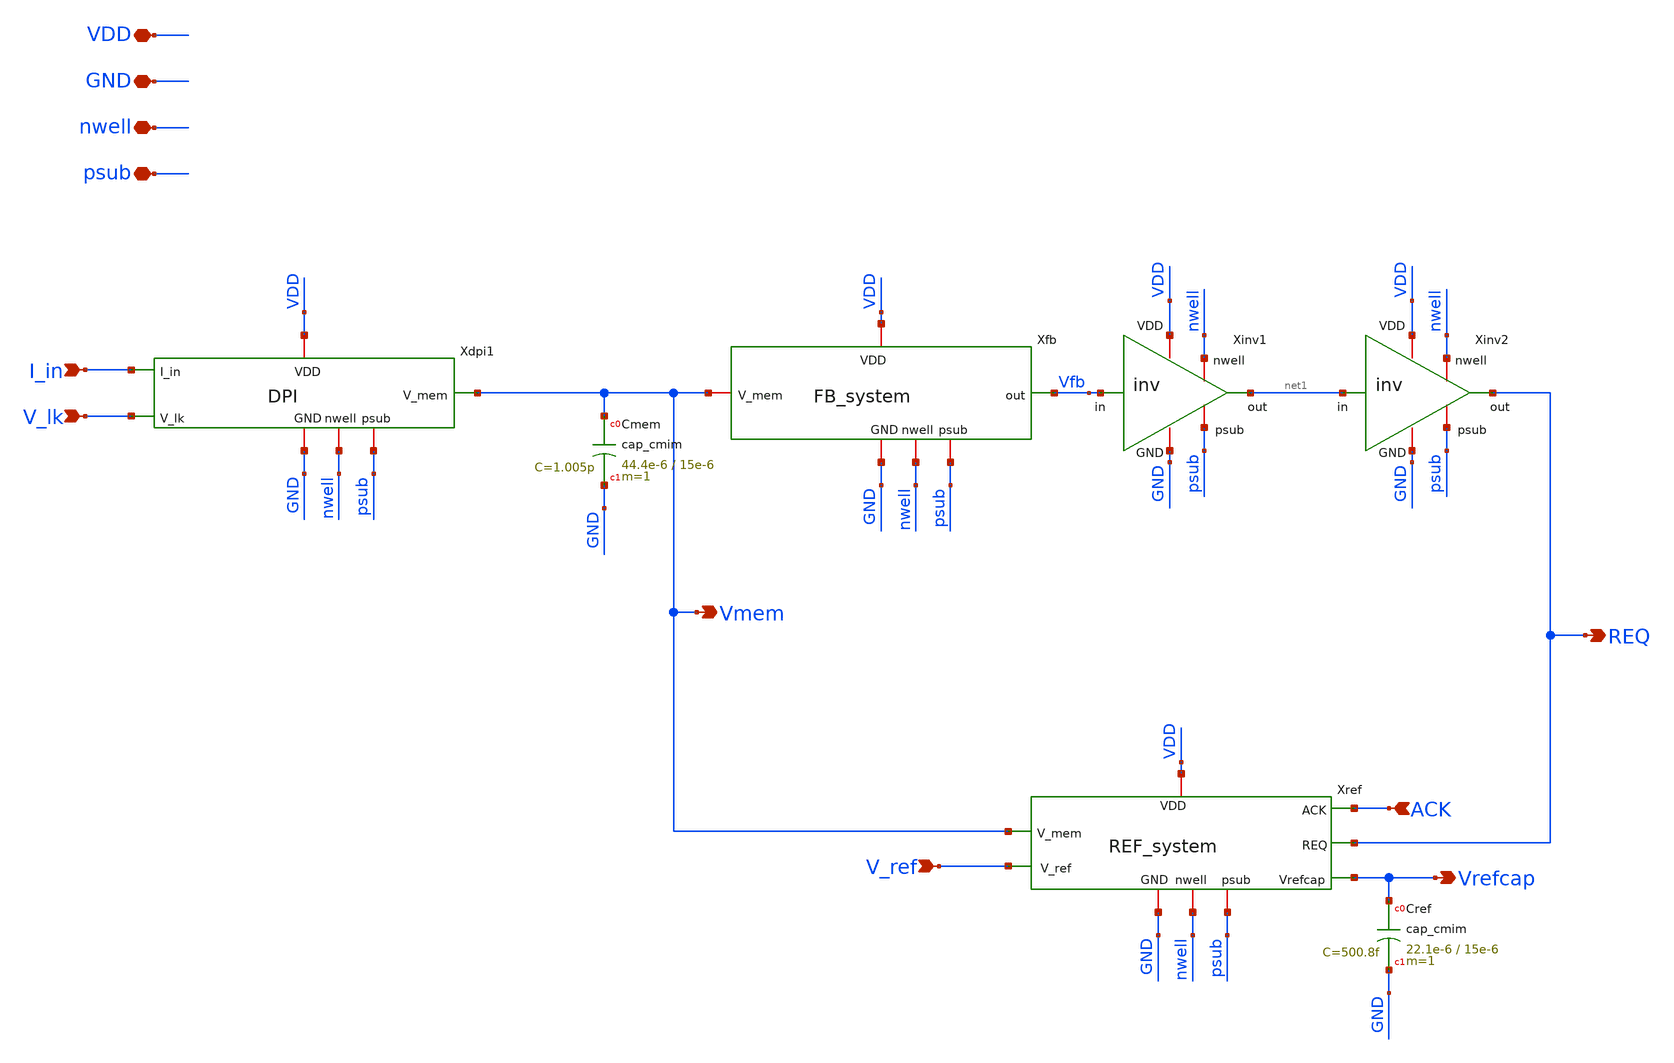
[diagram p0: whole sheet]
** sch_path: xschem/neuron_noahp.sch
**.subckt neuron_noahp V_ref GND VDD REQ ACK I_in V_lk Vmem Vrefcap psub nwell
*.ipin V_ref
*.iopin GND
*.iopin VDD
*.opin REQ
*.ipin ACK
*.ipin I_in
*.ipin V_lk
*.opin Vmem
*.opin Vrefcap
*.iopin psub
*.iopin nwell
Xinv1 VDD nwell net1 Vfb psub GND inv
Xinv2 VDD nwell REQ net1 psub GND inv
Xdpi1 I_in VDD Vmem V_lk GND nwell psub DPI
Xfb VDD Vfb Vmem GND nwell psub FB_system
Xref ACK Vmem REQ Vrefcap GND V_ref VDD nwell psub REF_system
XCmem Vmem GND cap_cmim w=44.4e-6 l=15e-6 m=1 mm_ok=1
XCref Vrefcap GND cap_cmim w=22.1e-6 l=15e-6 m=1 mm_ok=1
**.ends
.end
